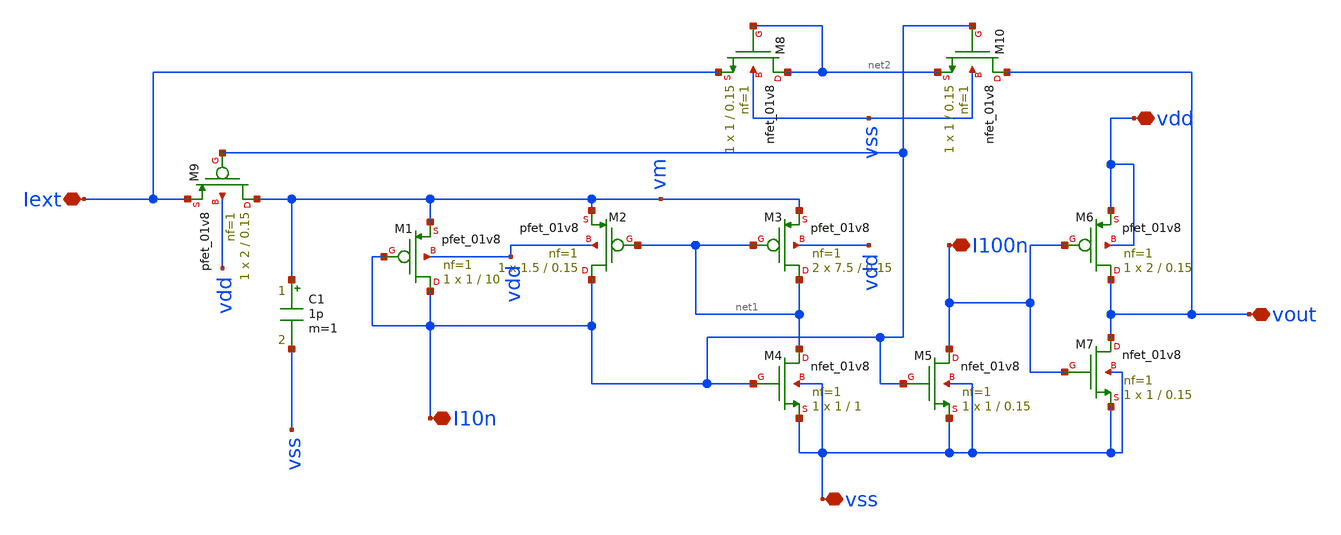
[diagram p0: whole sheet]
** sch_path: Neuron/ultralif/ultralif_retro.sch
**.subckt ultralif_retro Iext vout vss I10n vdd I100n
*.iopin Iext
*.iopin vout
*.iopin vss
*.iopin I10n
*.iopin vdd
*.iopin I100n
XM1 I10n I10n vm vdd sky130_fd_pr__pfet_01v8 L=10 W=1 nf=1 ad='int((nf+1)/2) * W/nf * 0.29' as='int((nf+2)/2) * W/nf * 0.29'
+ pd='2*int((nf+1)/2) * (W/nf + 0.29)' ps='2*int((nf+2)/2) * (W/nf + 0.29)' nrd='0.29 / W' nrs='0.29 / W'
+ sa=0 sb=0 sd=0 mult=1 m=1
XM2 I10n net1 vm vdd sky130_fd_pr__pfet_01v8 L=0.15 W=1.5 nf=1 ad='int((nf+1)/2) * W/nf * 0.29' as='int((nf+2)/2) * W/nf * 0.29'
+ pd='2*int((nf+1)/2) * (W/nf + 0.29)' ps='2*int((nf+2)/2) * (W/nf + 0.29)' nrd='0.29 / W' nrs='0.29 / W'
+ sa=0 sb=0 sd=0 mult=1 m=1
XM3 net1 net1 vm vdd sky130_fd_pr__pfet_01v8 L=0.15 W=7.5 nf=1 ad='int((nf+1)/2) * W/nf * 0.29' as='int((nf+2)/2) * W/nf * 0.29'
+ pd='2*int((nf+1)/2) * (W/nf + 0.29)' ps='2*int((nf+2)/2) * (W/nf + 0.29)' nrd='0.29 / W' nrs='0.29 / W'
+ sa=0 sb=0 sd=0 mult=2 m=2
XM4 net1 I10n vss vss sky130_fd_pr__nfet_01v8 L=1 W=1 nf=1 ad='int((1 + 1)/2) * 1 / 1 * 0.29' as='int((1 + 2)/2) * 1 / 1 * 0.29'
+ pd='2*int((1 + 1)/2) * (1 / 1 + 0.29)' ps='2*int((1 + 2)/2) * (1 / 1 + 0.29)' nrd='0.29 / 1 ' nrs='0.29 / 1 '
+ sa=0 sb=0 sd=0 mult=1 m=1
XM5 I100n I10n vss vss sky130_fd_pr__nfet_01v8 L=0.15 W=1 nf=1 ad='int((1 + 1)/2) * 1 / 1 * 0.29' as='int((1 + 2)/2) * 1 / 1 * 0.29'
+ pd='2*int((1 + 1)/2) * (1 / 1 + 0.29)' ps='2*int((1 + 2)/2) * (1 / 1 + 0.29)' nrd='0.29 / 1 ' nrs='0.29 / 1 '
+ sa=0 sb=0 sd=0 mult=1 m=1
XM6 vout I100n vdd vdd sky130_fd_pr__pfet_01v8 L=0.15 W=2 nf=1 ad='int((nf+1)/2) * W/nf * 0.29' as='int((nf+2)/2) * W/nf * 0.29'
+ pd='2*int((nf+1)/2) * (W/nf + 0.29)' ps='2*int((nf+2)/2) * (W/nf + 0.29)' nrd='0.29 / W' nrs='0.29 / W'
+ sa=0 sb=0 sd=0 mult=1 m=1
XM7 vout I100n vss vss sky130_fd_pr__nfet_01v8 L=0.15 W=1 nf=1 ad='int((1 + 1)/2) * 1 / 1 * 0.29' as='int((1 + 2)/2) * 1 / 1 * 0.29'
+ pd='2*int((1 + 1)/2) * (1 / 1 + 0.29)' ps='2*int((1 + 2)/2) * (1 / 1 + 0.29)' nrd='0.29 / 1 ' nrs='0.29 / 1 '
+ sa=0 sb=0 sd=0 mult=1 m=1
C1 vm vss 1p m=1
XM8 net2 net2 Iext vss sky130_fd_pr__nfet_01v8 L=0.15 W=1 nf=1 ad='int((1 + 1)/2) * 1 / 1 * 0.29' as='int((1 + 2)/2) * 1 / 1 * 0.29'
+ pd='2*int((1 + 1)/2) * (1 / 1 + 0.29)' ps='2*int((1 + 2)/2) * (1 / 1 + 0.29)' nrd='0.29 / 1 ' nrs='0.29 / 1 '
+ sa=0 sb=0 sd=0 mult=1 m=1
XM9 vm I10n Iext vdd sky130_fd_pr__pfet_01v8 L=0.15 W=2 nf=1 ad='int((nf+1)/2) * W/nf * 0.29' as='int((nf+2)/2) * W/nf * 0.29'
+ pd='2*int((nf+1)/2) * (W/nf + 0.29)' ps='2*int((nf+2)/2) * (W/nf + 0.29)' nrd='0.29 / W' nrs='0.29 / W'
+ sa=0 sb=0 sd=0 mult=1 m=1
XM10 vout I10n net2 vss sky130_fd_pr__nfet_01v8 L=0.15 W=1 nf=1 ad='int((1 + 1)/2) * 1 / 1 * 0.29' as='int((1 + 2)/2) * 1 / 1 * 0.29'
+ pd='2*int((1 + 1)/2) * (1 / 1 + 0.29)' ps='2*int((1 + 2)/2) * (1 / 1 + 0.29)' nrd='0.29 / 1 ' nrs='0.29 / 1 '
+ sa=0 sb=0 sd=0 mult=1 m=1
**.ends
.end
